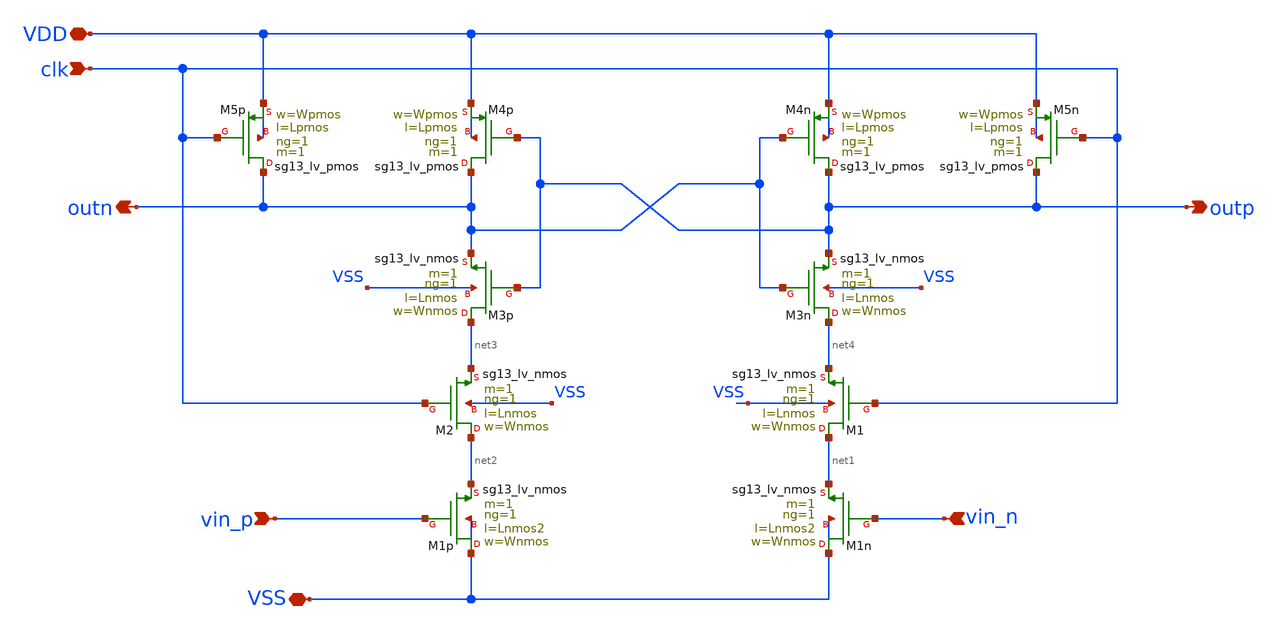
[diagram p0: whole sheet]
** sch_path: DSM/Schematics/new_comp/comp_test.sch
**.subckt comp_test clk VSS VDD vin_n vin_p outn outp
*.ipin clk
*.iopin VSS
*.iopin VDD
*.ipin vin_n
*.ipin vin_p
*.opin outn
*.opin outp
XM5p outn clk VDD VDD sg13_lv_pmos w=Wpmos l=Lpmos ng=1 m=1 mm_ok=1
XM4n outp outn VDD VDD sg13_lv_pmos w=Wpmos l=Lpmos ng=1 m=1 mm_ok=1
XM4p outn outp VDD VDD sg13_lv_pmos w=Wpmos l=Lpmos ng=1 m=1 mm_ok=1
XM5n outp clk VDD VDD sg13_lv_pmos w=Wpmos l=Lpmos ng=1 m=1 mm_ok=1
XM3p net3 outp outn VSS sg13_lv_nmos w=Wnmos l=Lnmos ng=1 m=1 mm_ok=1
XM3n net4 outn outp VSS sg13_lv_nmos w=Wnmos l=Lnmos ng=1 m=1 mm_ok=1
XM1n VSS vin_n net1 VSS sg13_lv_nmos w=Wnmos l=Lnmos2 ng=1 m=1 mm_ok=1
XM1p VSS vin_p net2 VSS sg13_lv_nmos w=Wnmos l=Lnmos2 ng=1 m=1 mm_ok=1
XM1 net1 clk net4 VSS sg13_lv_nmos w=Wnmos l=Lnmos ng=1 m=1 mm_ok=1
XM2 net2 clk net3 VSS sg13_lv_nmos w=Wnmos l=Lnmos ng=1 m=1 mm_ok=1
**.ends
.end
